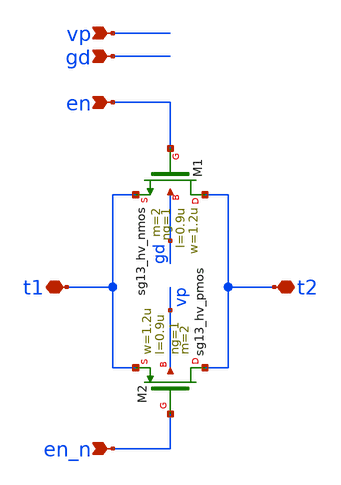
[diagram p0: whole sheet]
** sch_path: circuit/bandgap_bufor_tg.sch
**.subckt bandgap_bufor_tg en_n en vp gd t2 t1
*.ipin en_n
*.ipin en
*.ipin vp
*.ipin gd
*.iopin t2
*.iopin t1
XM1 t2 en t1 gd sg13_hv_nmos w=1.2u l=0.9u ng=1 m=2 mm_ok=1
XM2 t2 en_n t1 vp sg13_hv_pmos w=1.2u l=0.9u ng=1 m=2 mm_ok=1
**.ends
.end
